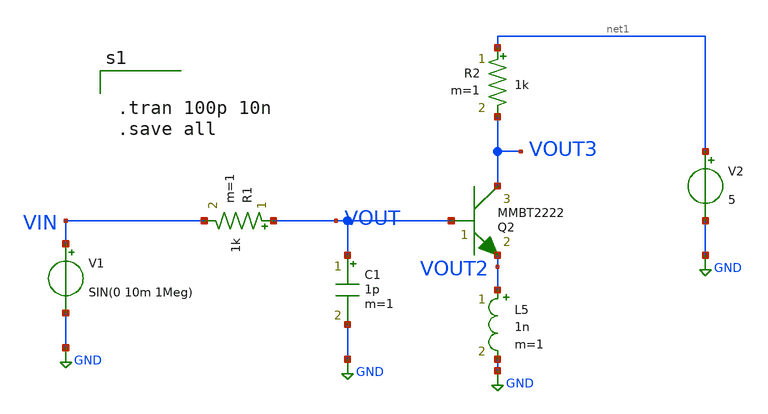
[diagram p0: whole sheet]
** sch_path: poweramp/poweramp2.sch
**.subckt poweramp2
R1 VOUT VIN 1k m=1
C1 VOUT GND 1p m=1
V1 VIN GND SIN(0 10m 1Meg)
V2 net1 GND 5
Q2 VOUT3 VOUT VOUT2 MMBT2222 area=1 m=1
L5 VOUT2 GND 1n m=1
R2 net1 VOUT3 1k m=1
**** begin user architecture code


.tran 100p 10n
.save all


**** end user architecture code
**.ends
.GLOBAL GND
.end
